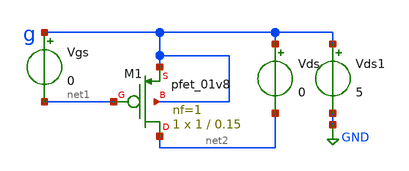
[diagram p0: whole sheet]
** sch_path: xschem/pmos_char.sch
**.subckt pmos_char
Vgs g net1 0
XM1 net2 net1 g g sky130_fd_pr__pfet_01v8 L=0.15 W=1 nf=1 ad='int((nf+1)/2) * W/nf * 0.29' as='int((nf+2)/2) * W/nf * 0.29'
+ pd='2*int((nf+1)/2) * (W/nf + 0.29)' ps='2*int((nf+2)/2) * (W/nf + 0.29)' nrd='0.29 / W' nrs='0.29 / W'
+ sa=0 sb=0 sd=0 mult=1 m=1
Vds g net2 0
Vds1 g GND 5
**** begin user architecture code
 .lib $::SKYWATER_MODELS/sky130.lib.spice tt


.dc Vds 0 1.8 1m Vgs 0 5 0.5
.save all


**** end user architecture code
**.ends
.GLOBAL GND
.end
